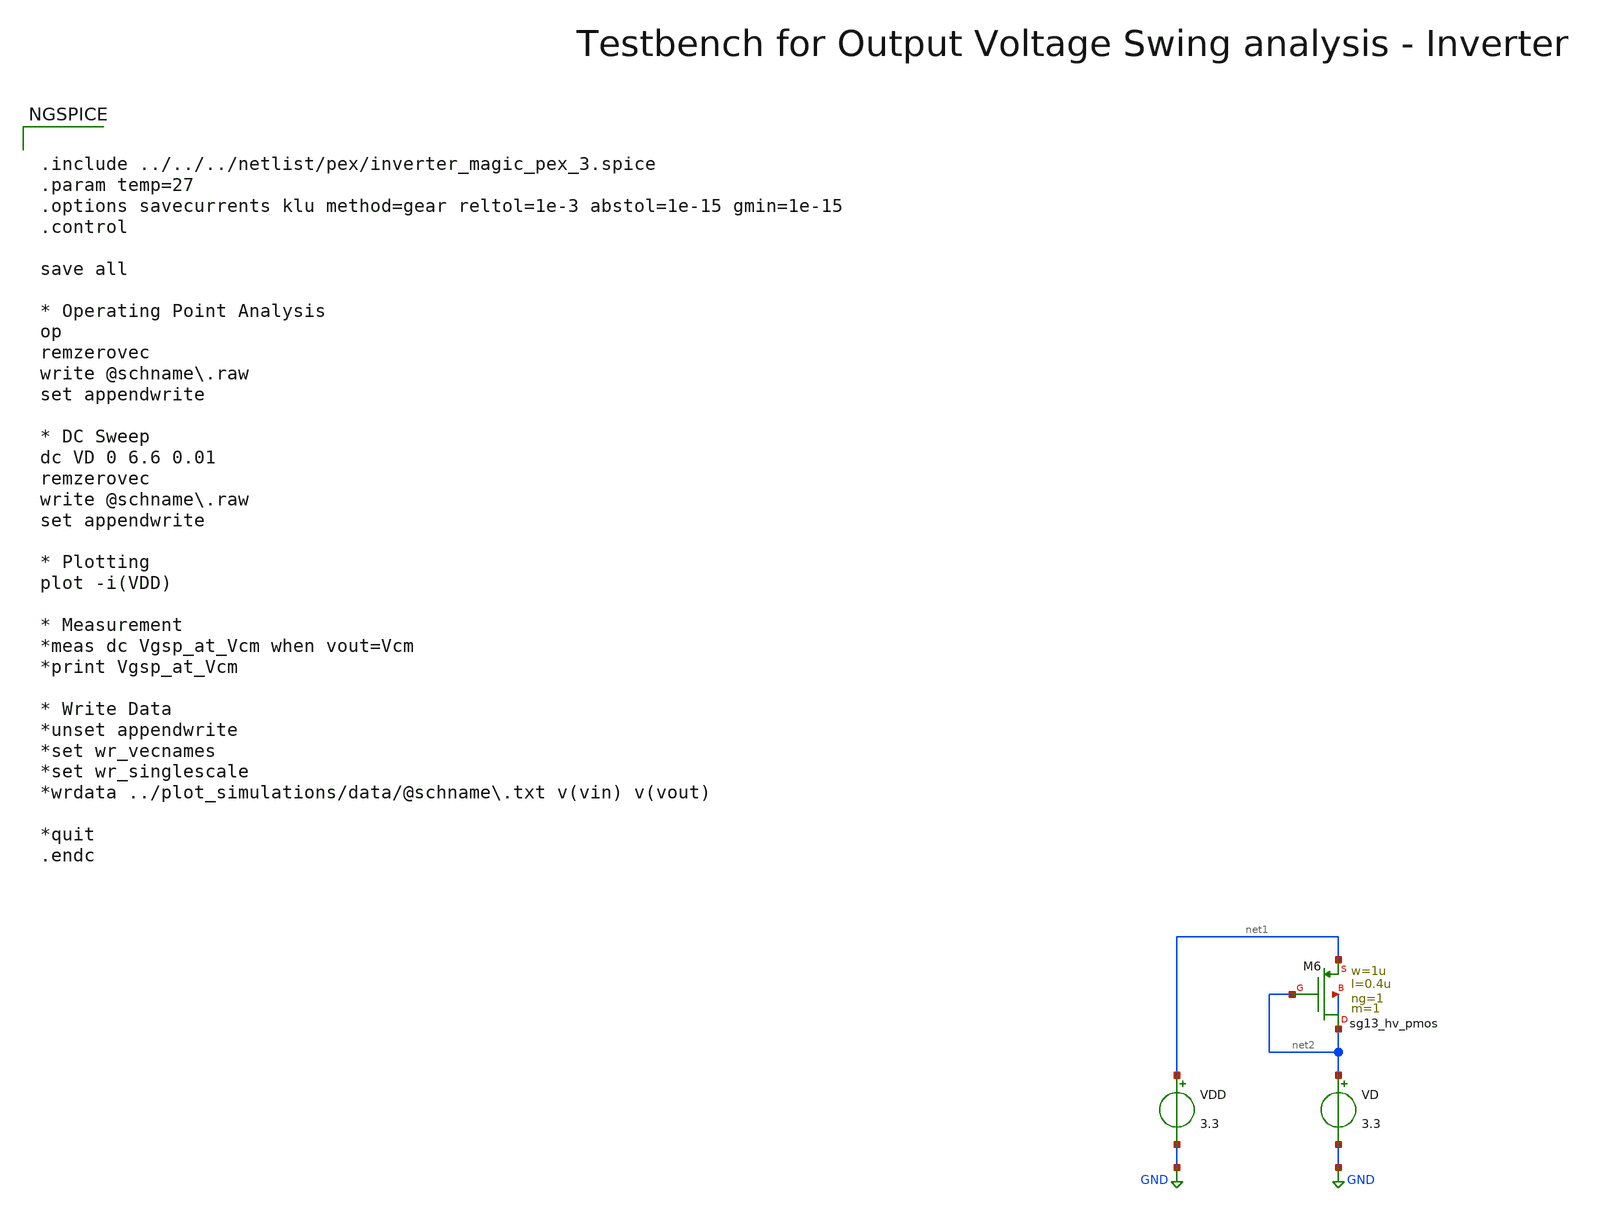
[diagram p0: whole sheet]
** sch_path: macros/heichips26_vcr/macros/switched_capacitor/testbenches/xschem/tb_pmos_diode_dc.sch
**.subckt tb_pmos_diode_dc
VDD net1 GND 3.3
XM6 net2 net2 net1 net2 sg13_hv_pmos w=1u l=0.4u ng=1 m=1 mm_ok=1
VD net2 GND 3.3
**** begin user architecture code


.include ../../../netlist/pex/inverter_magic_pex_3.spice
.param temp=27
.options savecurrents klu method=gear reltol=1e-3 abstol=1e-15 gmin=1e-15
.control

save all

* Operating Point Analysis
op
remzerovec
write @schname\.raw
set appendwrite

* DC Sweep
dc VD 0 6.6 0.01
remzerovec
write @schname\.raw
set appendwrite

* Plotting
plot -i(VDD)

* Measurement
*meas dc Vgsp_at_Vcm when vout=Vcm
*print Vgsp_at_Vcm

* Write Data
*unset appendwrite
*set wr_vecnames
*set wr_singlescale
*wrdata ../plot_simulations/data/@schname\.txt v(vin) v(vout)

*quit
.endc



.lib cornerMOSlv.lib mos_tt
.lib cornerMOShv.lib mos_tt
.lib cornerRES.lib res_typ
.lib cornerDIO.lib dio_tt

**** end user architecture code
**.ends
.GLOBAL GND
.end
